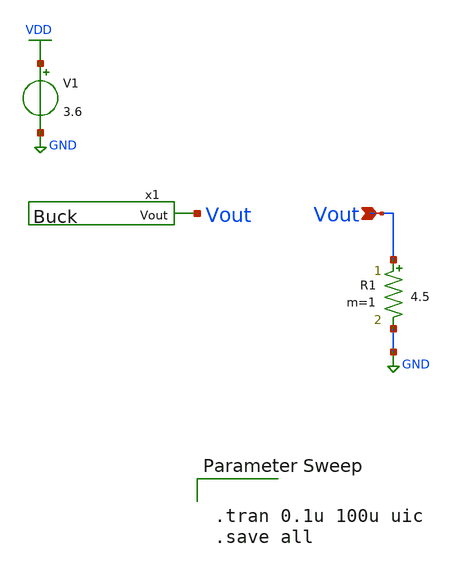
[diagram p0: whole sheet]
** sch_path: Ene_Thompson/test_Buck.sch
**.subckt test_Buck Vout
*.ipin Vout
x1 Vout Buck
V1 VDD GND 3.6
R1 Vout GND 4.5 m=1
**** begin user architecture code

.lib $::SKYWATER_MODELS/sky130.lib.spice tt



.tran 0.1u 100u uic
.save all


**** end user architecture code
**.ends

* expanding   symbol:  Buck.sym # of pins=1
** sym_path: Ene_Thompson/Buck.sym
** sch_path: Ene_Thompson/Buck.sch
.subckt Buck Vout
*.opin Vout
XM1 vl net1 VDD VDD sky130_fd_pr__pfet_g5v0d10v5 L=0.5 W=20 nf=1 ad='int((nf+1)/2) * W/nf * 0.29' as='int((nf+2)/2) * W/nf * 0.29'
+ pd='2*int((nf+1)/2) * (W/nf + 0.29)' ps='2*int((nf+2)/2) * (W/nf + 0.29)' nrd='0.29 / W' nrs='0.29 / W'
+ sa=0 sb=0 sd=0 mult=1000 m=1000
XM2 vl net2 GND GND sky130_fd_pr__nfet_g5v0d10v5 L=0.5 W=20 nf=1 ad='int((nf+1)/2) * W/nf * 0.29' as='int((nf+2)/2) * W/nf * 0.29'
+ pd='2*int((nf+1)/2) * (W/nf + 0.29)' ps='2*int((nf+2)/2) * (W/nf + 0.29)' nrd='0.29 / W' nrs='0.29 / W'
+ sa=0 sb=0 sd=0 mult=1000 m=1000
L1 vl Vout 4.7u m=1
C1 Vout GND 1u m=1
V1 net1 GND PULSE(0 5 0 1n 1n 0.1u 0.2u)
V2 net2 GND PULSE(0 5 0 1n 1n 0.1u 0.2u)
.ends

.GLOBAL VDD
.GLOBAL GND
.end
